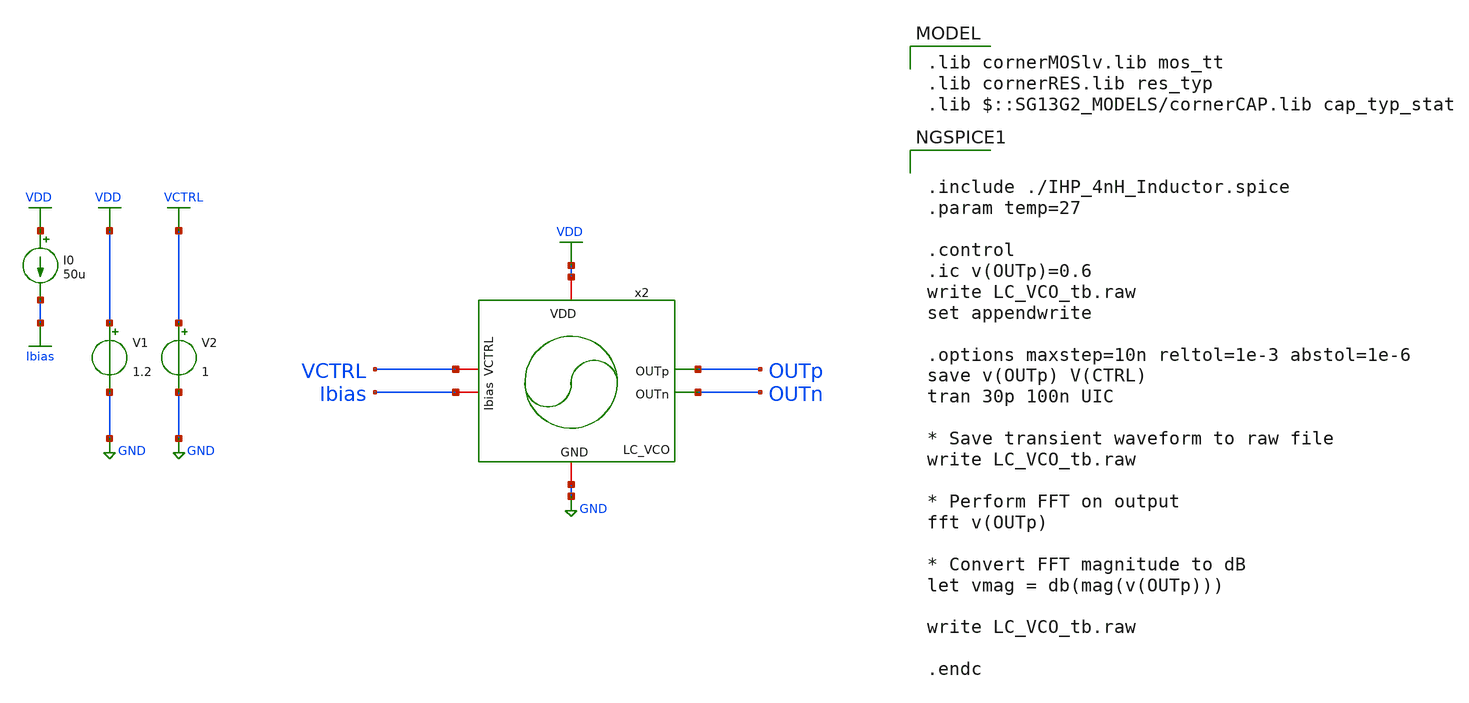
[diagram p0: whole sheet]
** sch_path: schematic/blocks/lc-vco/LC_VCO_tb.sch
**.subckt LC_VCO_tb
V1 VDD GND 1.2
V2 VCTRL GND 1
I0 VDD Ibias 50u
x2 VDD OUTp OUTn Ibias VCTRL GND LC_VCO
**** begin user architecture code
 .lib cornerMOSlv.lib mos_tt
.lib cornerRES.lib res_typ
.lib $::SG13G2_MODELS/cornerCAP.lib cap_typ_stat



.include ./IHP_4nH_Inductor.spice
.param temp=27

.control
.ic v(OUTp)=0.6
write LC_VCO_tb.raw
set appendwrite

.options maxstep=10n reltol=1e-3 abstol=1e-6
save v(OUTp) V(CTRL)
tran 30p 100n UIC

* Save transient waveform to raw file
write LC_VCO_tb.raw

* Perform FFT on output
fft v(OUTp)

* Convert FFT magnitude to dB
let vmag = db(mag(v(OUTp)))

write LC_VCO_tb.raw

.endc


**** end user architecture code
**.ends
.GLOBAL GND
.GLOBAL VDD
.GLOBAL VCTRL
.GLOBAL Ibias
.end
